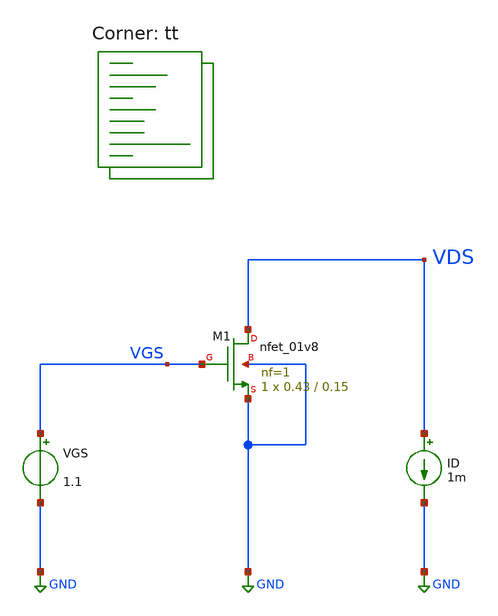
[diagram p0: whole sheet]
** sch_path: projects/bandgapref/xschem_ngspice/new_files/gm_id_check_3.sch
**.subckt gm_id_check_3
XM1 VDS VGS GND GND sky130_fd_pr__nfet_01v8 L=0.15 W=0.43 nf=1 ad='int((nf+1)/2) * W/nf * 0.29' as='int((nf+2)/2) * W/nf * 0.29'
+ pd='2*int((nf+1)/2) * (W/nf + 0.29)' ps='2*int((nf+2)/2) * (W/nf + 0.29)' nrd='0.29 / W' nrs='0.29 / W'
+ sa=0 sb=0 sd=0 mult=1 m=1
VGS VGS GND 1.1
ID VDS GND 1m
**** begin user architecture code
.lib $::SKYWATER_MODELS/sky130.lib.spice tt



.option method=gear
.option wnflag=1
.option savecurrents

.save @m.xm1.msky130_fd_pr__nfet_01v8[gm]

.control
  save all
  *  dc VGS 0 1.8 0.1 VDS 0 1.8 0.1
  dc ID 0 1m 1u VGS 0 1.8 0.1
  remzerovec
  write gm_id_check_3.raw
  set appendwrite
.endc



**** end user architecture code
**.ends
.GLOBAL GND
.end
